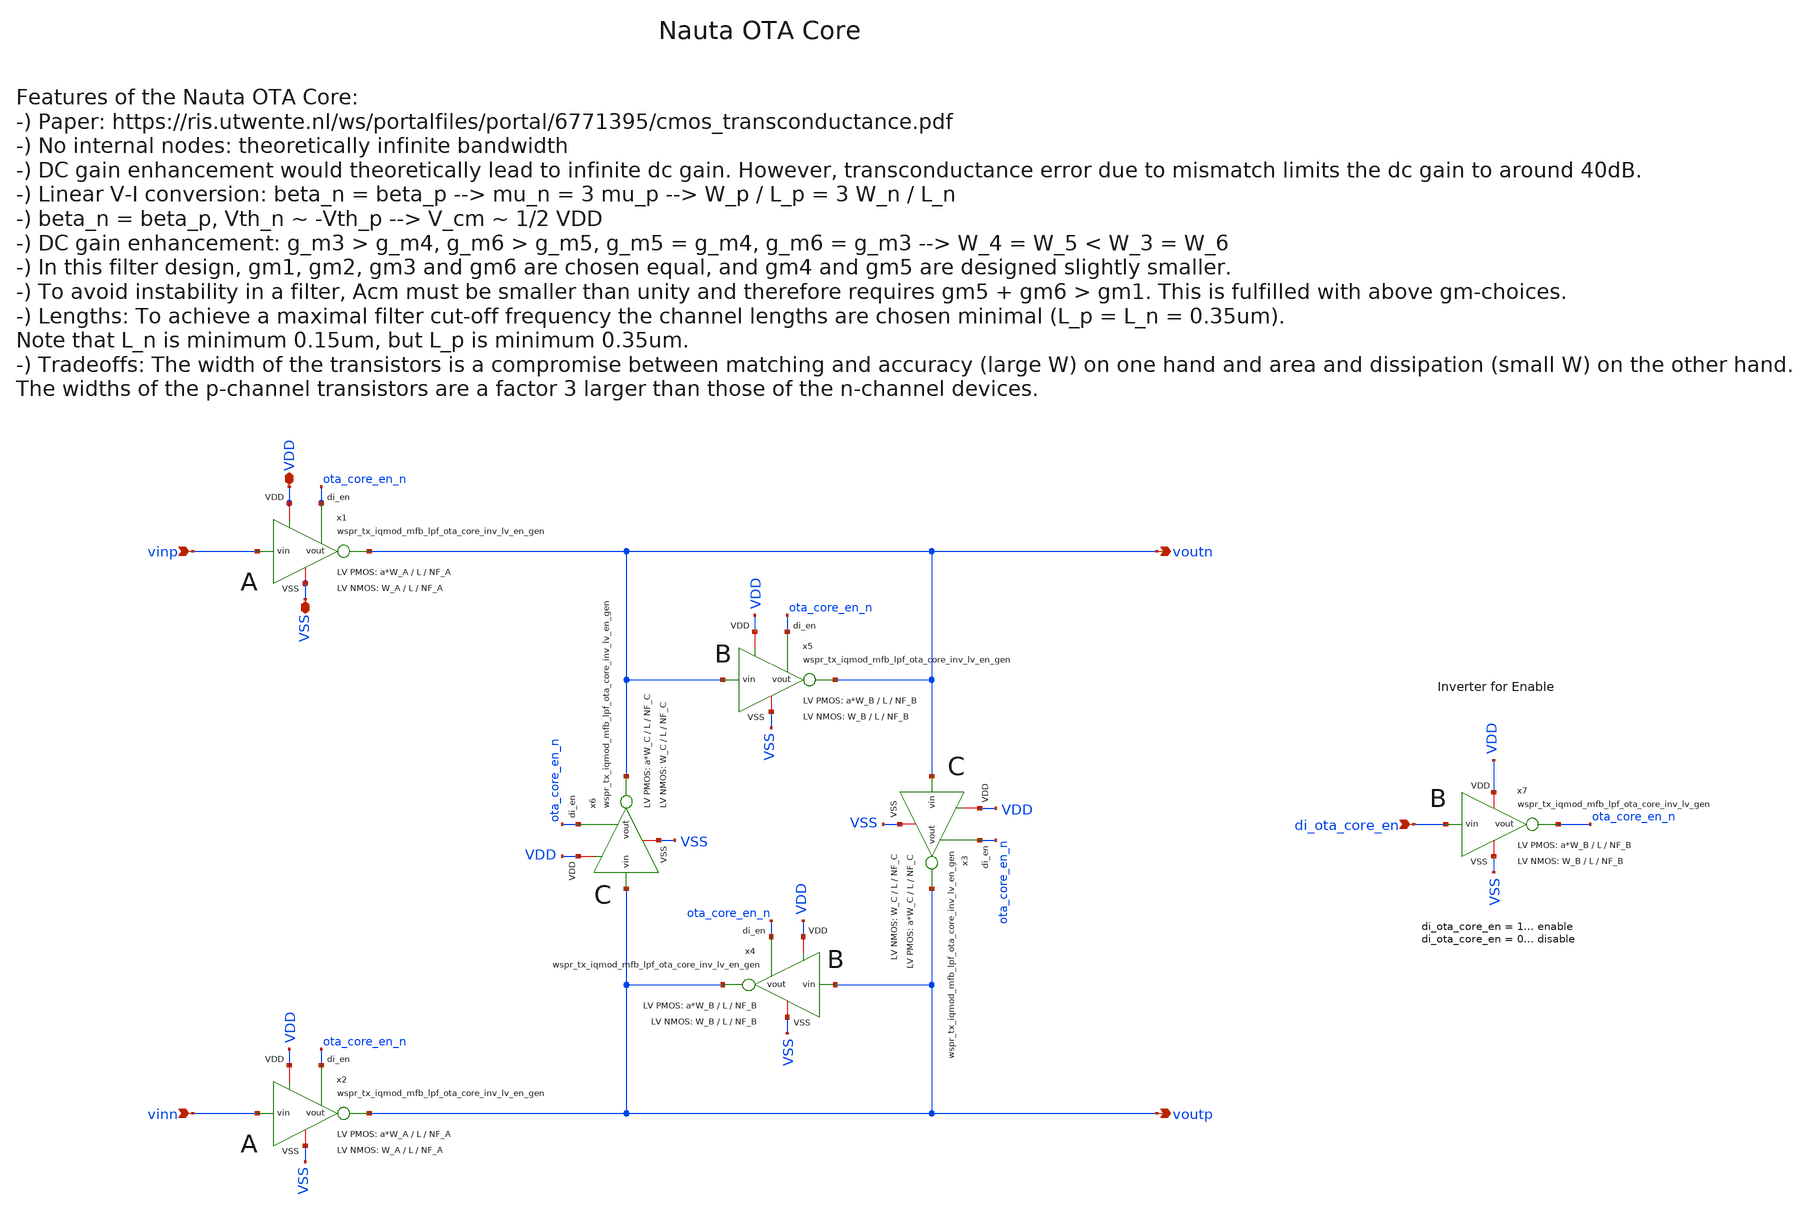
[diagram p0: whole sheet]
** sch_path: sky130/xschem/generic/wspr_tx_iqmod_mfb_lpf_ota_core_nauta_gen.sch
**.subckt wspr_tx_iqmod_mfb_lpf_ota_core_nauta_gen di_ota_core_en vinp vinn voutp voutn VDD VSS
*.ipin di_ota_core_en
*.ipin vinp
*.ipin vinn
*.opin voutp
*.opin voutn
*.iopin VDD
*.iopin VSS
x7 VDD di_ota_core_en ota_core_en_n VSS wspr_tx_iqmod_mfb_lpf_ota_core_inv_lv_gen W_P=a*W_B L_P=L
+ NF_P=NF_B W_N=W_B L_N=L NF_N=NF_B
x2 VDD vinn voutp VSS ota_core_en_n wspr_tx_iqmod_mfb_lpf_ota_core_inv_lv_en_gen W_P=a*W_A L_P=L
+ NF_P=NF_A W_N=W_A L_N=L NF_N=NF_A
x1 VDD vinp voutn VSS ota_core_en_n wspr_tx_iqmod_mfb_lpf_ota_core_inv_lv_en_gen W_P=a*W_A L_P=L
+ NF_P=NF_A W_N=W_A L_N=L NF_N=NF_A
x4 VDD voutp voutp VSS ota_core_en_n wspr_tx_iqmod_mfb_lpf_ota_core_inv_lv_en_gen W_P=a*W_B L_P=L
+ NF_P=NF_B W_N=W_B L_N=L NF_N=NF_B
x5 VDD voutn voutn VSS ota_core_en_n wspr_tx_iqmod_mfb_lpf_ota_core_inv_lv_en_gen W_P=a*W_B L_P=L
+ NF_P=NF_B W_N=W_B L_N=L NF_N=NF_B
x6 VDD voutp voutn VSS ota_core_en_n wspr_tx_iqmod_mfb_lpf_ota_core_inv_lv_en_gen W_P=a*W_C L_P=L
+ NF_P=NF_C W_N=W_C L_N=L NF_N=NF_C
x3 VDD voutn voutp VSS ota_core_en_n wspr_tx_iqmod_mfb_lpf_ota_core_inv_lv_en_gen W_P=a*W_C L_P=L
+ NF_P=NF_C W_N=W_C L_N=L NF_N=NF_C
**.ends
.end
